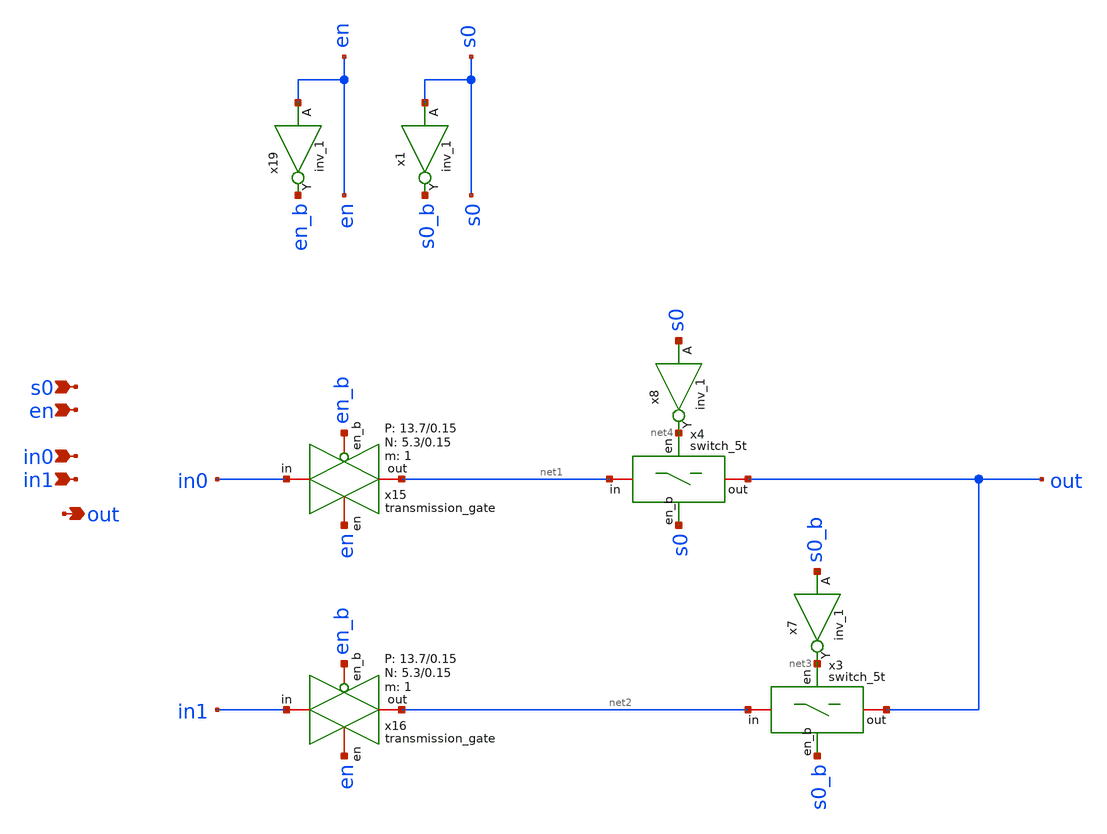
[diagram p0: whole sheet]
** sch_path: design/analog_modulator/schematic/a_mux2_en.sch
**.subckt a_mux2_en en s0 in0 in1 out
*.ipin en
*.ipin s0
*.ipin in0
*.ipin in1
*.opin out
x3 net2 out net3 s0_b VDD VSS switch_5t
x4 net1 out net4 s0 VDD VSS switch_5t
x7 s0_b VSS VSS VDD VDD net3 sky130_fd_sc_hd__inv_1
x8 s0 VSS VSS VDD VDD net4 sky130_fd_sc_hd__inv_1
x15 in0 net1 en en_b VDD VSS 1 5.3 0.15 13.7 0.15 transmission_gate
x16 in1 net2 en en_b VDD VSS 1 5.3 0.15 13.7 0.15 transmission_gate
x19 en VSS VSS VDD VDD en_b sky130_fd_sc_hd__inv_1
x1 s0 VSS VSS VDD VDD s0_b sky130_fd_sc_hd__inv_1
**.ends

* expanding   symbol:  switch_5t.sym # of pins=4
** sym_path: design/analog_modulator/schematic/switch_5t.sym
** sch_path: design/analog_modulator/schematic/switch_5t.sch
.subckt switch_5t in out en en_b VDD VSS
*.iopin in
*.iopin out
*.ipin en
*.ipin en_b
x1 in net1 en en_b VDD VSS 1 5.3 0.15 13.7 0.15 transmission_gate
x2 net1 out en en_b VDD VSS 1 5.3 0.15 13.7 0.15 transmission_gate
XM1 net1 en_b VSS VSS sky130_fd_pr__nfet_01v8 L=0.15 W=0.5 nf=1 ad='int((nf+1)/2) * W/nf * 0.29' as='int((nf+2)/2) * W/nf * 0.29'
+ pd='2*int((nf+1)/2) * (W/nf + 0.29)' ps='2*int((nf+2)/2) * (W/nf + 0.29)' nrd='0.29 / W' nrs='0.29 / W'
+ sa=0 sb=0 sd=0 mult=1 m=1
.ends


* expanding   symbol:  transmission_gate.sym # of pins=4
** sym_path: design/analog_modulator/schematic/transmission_gate.sym
** sch_path: design/analog_modulator/schematic/transmission_gate.sch
.subckt transmission_gate in out en en_b VDD VSS N W_N L_N W_P L_P    N=1 W_N=5.3 L_N=0.15 W_P=13.7
+ L_P=0.15
*.iopin in
*.iopin out
*.ipin en
*.ipin en_b
XM1 out en in VSS sky130_fd_pr__nfet_01v8 L='L_N' W='W_N' nf=1 ad='int((nf+1)/2) * W/nf * 0.29' as='int((nf+2)/2) * W/nf * 0.29'
+ pd='2*int((nf+1)/2) * (W/nf + 0.29)' ps='2*int((nf+2)/2) * (W/nf + 0.29)' nrd='0.29 / W' nrs='0.29 / W'
+ sa=0 sb=0 sd=0 mult='N' m='N'
XM2 out en_b in VDD sky130_fd_pr__pfet_01v8 L='L_P' W='W_P' nf=1 ad='int((nf+1)/2) * W/nf * 0.29' as='int((nf+2)/2) * W/nf * 0.29'
+ pd='2*int((nf+1)/2) * (W/nf + 0.29)' ps='2*int((nf+2)/2) * (W/nf + 0.29)' nrd='0.29 / W' nrs='0.29 / W'
+ sa=0 sb=0 sd=0 mult='N' m='N'
.ends

.end
